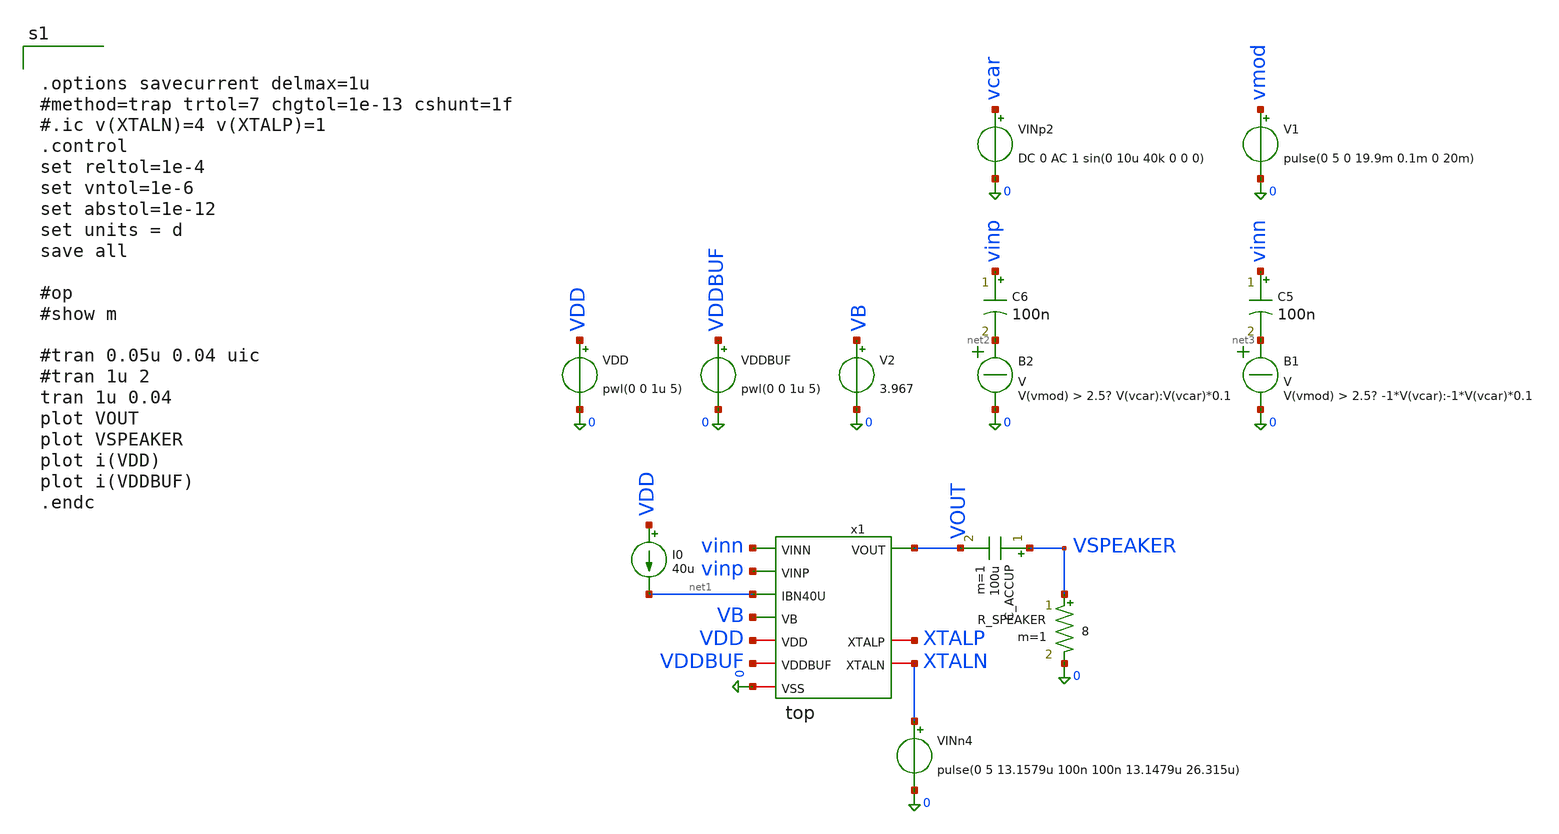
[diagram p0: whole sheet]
** sch_path: member_project/JJY_Receiver/Masahiro/jjy_recv/system_sim/top_sym.sch
**.subckt top_sym
I0 VDD net1 40u
R_SPEAKER VSPEAKER 0 8 m=1
C_ACCUP VSPEAKER VOUT 100u m=1
V2 VB 0 3.967
VINp2 vcar 0 DC 0 AC 1 sin(0 10u 40k 0 0 0)
V1 vmod 0 pulse(0 5 0 19.9m 0.1m 0 20m)
B2 net2 0 V = V(vmod) > 2.5? V(vcar):V(vcar)*0.1
B1 net3 0 V = V(vmod) > 2.5? -1*V(vcar):-1*V(vcar)*0.1
C5 vinn net3 100n m=1
C6 vinp net2 100n m=1
VDDBUF VDDBUF 0 pwl(0 0 1u 5)
VDD VDD 0 pwl(0 0 1u 5)
x1 XTALP VDD 0 XTALN net1 VB VOUT vinn vinp VDDBUF top
VINn4 XTALN 0 pulse(0 5 13.1579u 100n 100n 13.1479u 26.315u)
**** begin user architecture code
 .include $::LIB/ip62_models


.options savecurrent delmax=1u
#method=trap trtol=7 chgtol=1e-13 cshunt=1f
#.ic v(XTALN)=4 v(XTALP)=1
.control
set reltol=1e-4
set vntol=1e-6
set abstol=1e-12
set units = d
save all

#op
#show m

#tran 0.05u 0.04 uic
#tran 1u 2
tran 1u 0.04
plot VOUT
plot VSPEAKER
plot i(VDD)
plot i(VDDBUF)
.endc


**** end user architecture code
**.ends
.end
